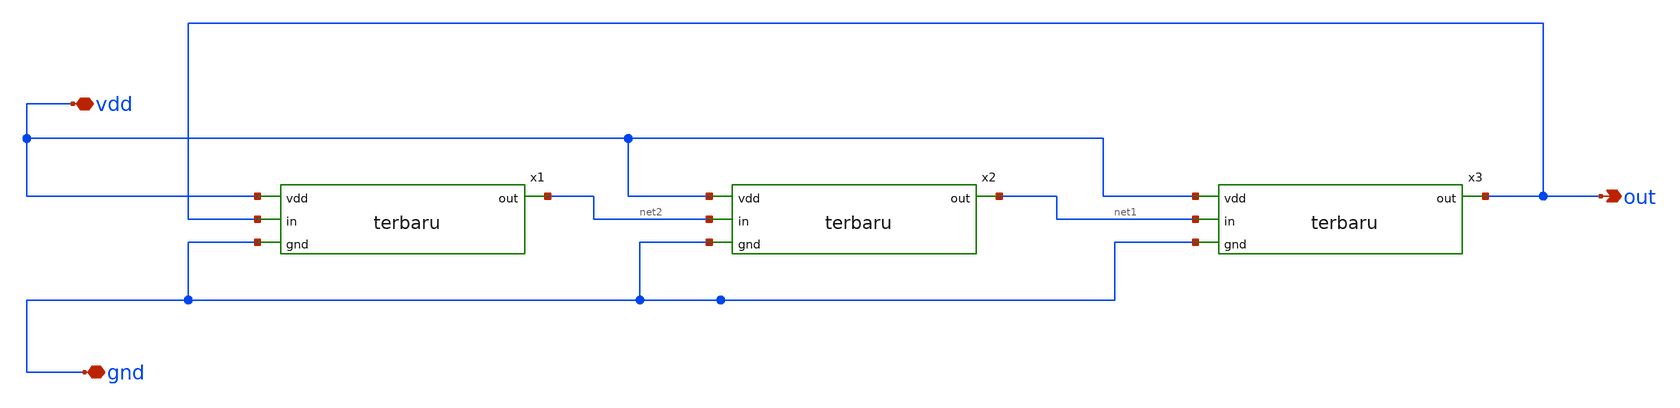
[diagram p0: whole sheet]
** sch_path: ringosi/ringosi/ringosibasic.sch
**.subckt ringosibasic vdd gnd out
*.iopin vdd
*.iopin gnd
*.opin out
x1 vdd out net2 gnd terbaru
x2 vdd net2 net1 gnd terbaru
x3 vdd net1 out gnd terbaru
**.ends
.end
